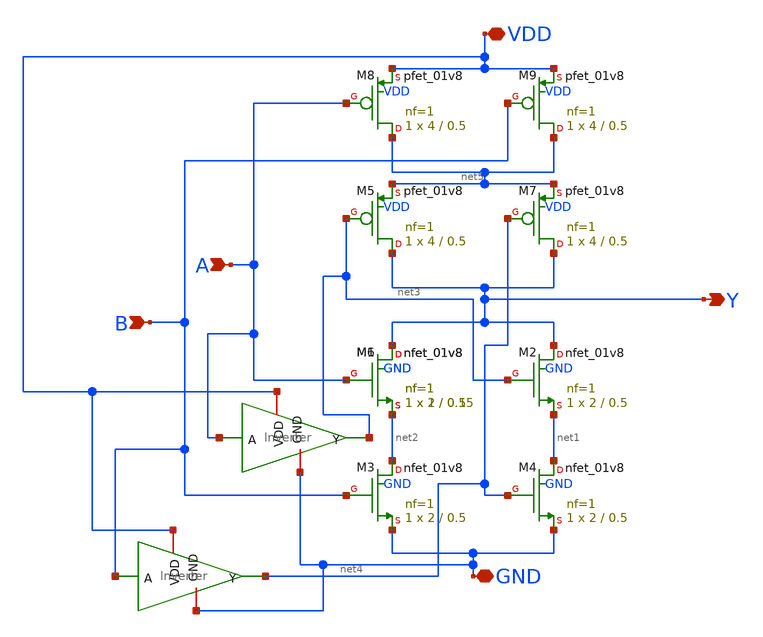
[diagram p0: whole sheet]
** sch_path: XOR/XOR.sch
**.subckt XOR A B Y GND VDD
*.ipin A
*.ipin B
*.opin Y
*.iopin GND
*.iopin VDD
XM1 Y A net2 GND sky130_fd_pr__nfet_01v8 L=0.5 W=2 nf=1 ad='int((nf+1)/2) * W/nf * 0.29' as='int((nf+2)/2) * W/nf * 0.29'
+ pd='2*int((nf+1)/2) * (W/nf + 0.29)' ps='2*int((nf+2)/2) * (W/nf + 0.29)' nrd='0.29 / W' nrs='0.29 / W'
+ sa=0 sb=0 sd=0 mult=1 m=1
XM2 Y net3 net1 GND sky130_fd_pr__nfet_01v8 L=0.5 W=2 nf=1 ad='int((nf+1)/2) * W/nf * 0.29' as='int((nf+2)/2) * W/nf * 0.29'
+ pd='2*int((nf+1)/2) * (W/nf + 0.29)' ps='2*int((nf+2)/2) * (W/nf + 0.29)' nrd='0.29 / W' nrs='0.29 / W'
+ sa=0 sb=0 sd=0 mult=1 m=1
XM3 net2 B GND GND sky130_fd_pr__nfet_01v8 L=0.5 W=2 nf=1 ad='int((nf+1)/2) * W/nf * 0.29' as='int((nf+2)/2) * W/nf * 0.29'
+ pd='2*int((nf+1)/2) * (W/nf + 0.29)' ps='2*int((nf+2)/2) * (W/nf + 0.29)' nrd='0.29 / W' nrs='0.29 / W'
+ sa=0 sb=0 sd=0 mult=1 m=1
XM4 net1 net4 GND GND sky130_fd_pr__nfet_01v8 L=0.5 W=2 nf=1 ad='int((nf+1)/2) * W/nf * 0.29' as='int((nf+2)/2) * W/nf * 0.29'
+ pd='2*int((nf+1)/2) * (W/nf + 0.29)' ps='2*int((nf+2)/2) * (W/nf + 0.29)' nrd='0.29 / W' nrs='0.29 / W'
+ sa=0 sb=0 sd=0 mult=1 m=1
XM5 Y net3 net5 VDD sky130_fd_pr__pfet_01v8 L=0.5 W=4 nf=1 ad='int((nf+1)/2) * W/nf * 0.29' as='int((nf+2)/2) * W/nf * 0.29'
+ pd='2*int((nf+1)/2) * (W/nf + 0.29)' ps='2*int((nf+2)/2) * (W/nf + 0.29)' nrd='0.29 / W' nrs='0.29 / W'
+ sa=0 sb=0 sd=0 mult=1 m=1
XM6 Y A net2 GND sky130_fd_pr__nfet_01v8 L=0.15 W=1 nf=1 ad='int((nf+1)/2) * W/nf * 0.29' as='int((nf+2)/2) * W/nf * 0.29'
+ pd='2*int((nf+1)/2) * (W/nf + 0.29)' ps='2*int((nf+2)/2) * (W/nf + 0.29)' nrd='0.29 / W' nrs='0.29 / W'
+ sa=0 sb=0 sd=0 mult=1 m=1
XM7 Y net4 net5 VDD sky130_fd_pr__pfet_01v8 L=0.5 W=4 nf=1 ad='int((nf+1)/2) * W/nf * 0.29' as='int((nf+2)/2) * W/nf * 0.29'
+ pd='2*int((nf+1)/2) * (W/nf + 0.29)' ps='2*int((nf+2)/2) * (W/nf + 0.29)' nrd='0.29 / W' nrs='0.29 / W'
+ sa=0 sb=0 sd=0 mult=1 m=1
XM8 net5 A VDD VDD sky130_fd_pr__pfet_01v8 L=0.5 W=4 nf=1 ad='int((nf+1)/2) * W/nf * 0.29' as='int((nf+2)/2) * W/nf * 0.29'
+ pd='2*int((nf+1)/2) * (W/nf + 0.29)' ps='2*int((nf+2)/2) * (W/nf + 0.29)' nrd='0.29 / W' nrs='0.29 / W'
+ sa=0 sb=0 sd=0 mult=1 m=1
XM9 net5 B VDD VDD sky130_fd_pr__pfet_01v8 L=0.5 W=4 nf=1 ad='int((nf+1)/2) * W/nf * 0.29' as='int((nf+2)/2) * W/nf * 0.29'
+ pd='2*int((nf+1)/2) * (W/nf + 0.29)' ps='2*int((nf+2)/2) * (W/nf + 0.29)' nrd='0.29 / W' nrs='0.29 / W'
+ sa=0 sb=0 sd=0 mult=1 m=1
x1 VDD A net3 GND Inverter
x2 VDD B net4 GND Inverter
**.ends

* expanding   symbol:  /home/ee431/workspace/inverter/Inverter.sym # of pins=4
** sym_path: inverter/Inverter.sym
** sch_path: inverter/Inverter.sch
.subckt Inverter VDD A Y GND
*.ipin A
*.opin Y
*.iopin VDD
*.iopin GND
XM1 Y A VDD VDD sky130_fd_pr__pfet_01v8 L=0.5 W=2 nf=1 ad='int((nf+1)/2) * W/nf * 0.29' as='int((nf+2)/2) * W/nf * 0.29'
+ pd='2*int((nf+1)/2) * (W/nf + 0.29)' ps='2*int((nf+2)/2) * (W/nf + 0.29)' nrd='0.29 / W' nrs='0.29 / W'
+ sa=0 sb=0 sd=0 mult=1 m=1
XM2 Y A GND GND sky130_fd_pr__nfet_01v8 L=0.5 W=1 nf=1 ad='int((nf+1)/2) * W/nf * 0.29' as='int((nf+2)/2) * W/nf * 0.29'
+ pd='2*int((nf+1)/2) * (W/nf + 0.29)' ps='2*int((nf+2)/2) * (W/nf + 0.29)' nrd='0.29 / W' nrs='0.29 / W'
+ sa=0 sb=0 sd=0 mult=1 m=1
.ends

.end
